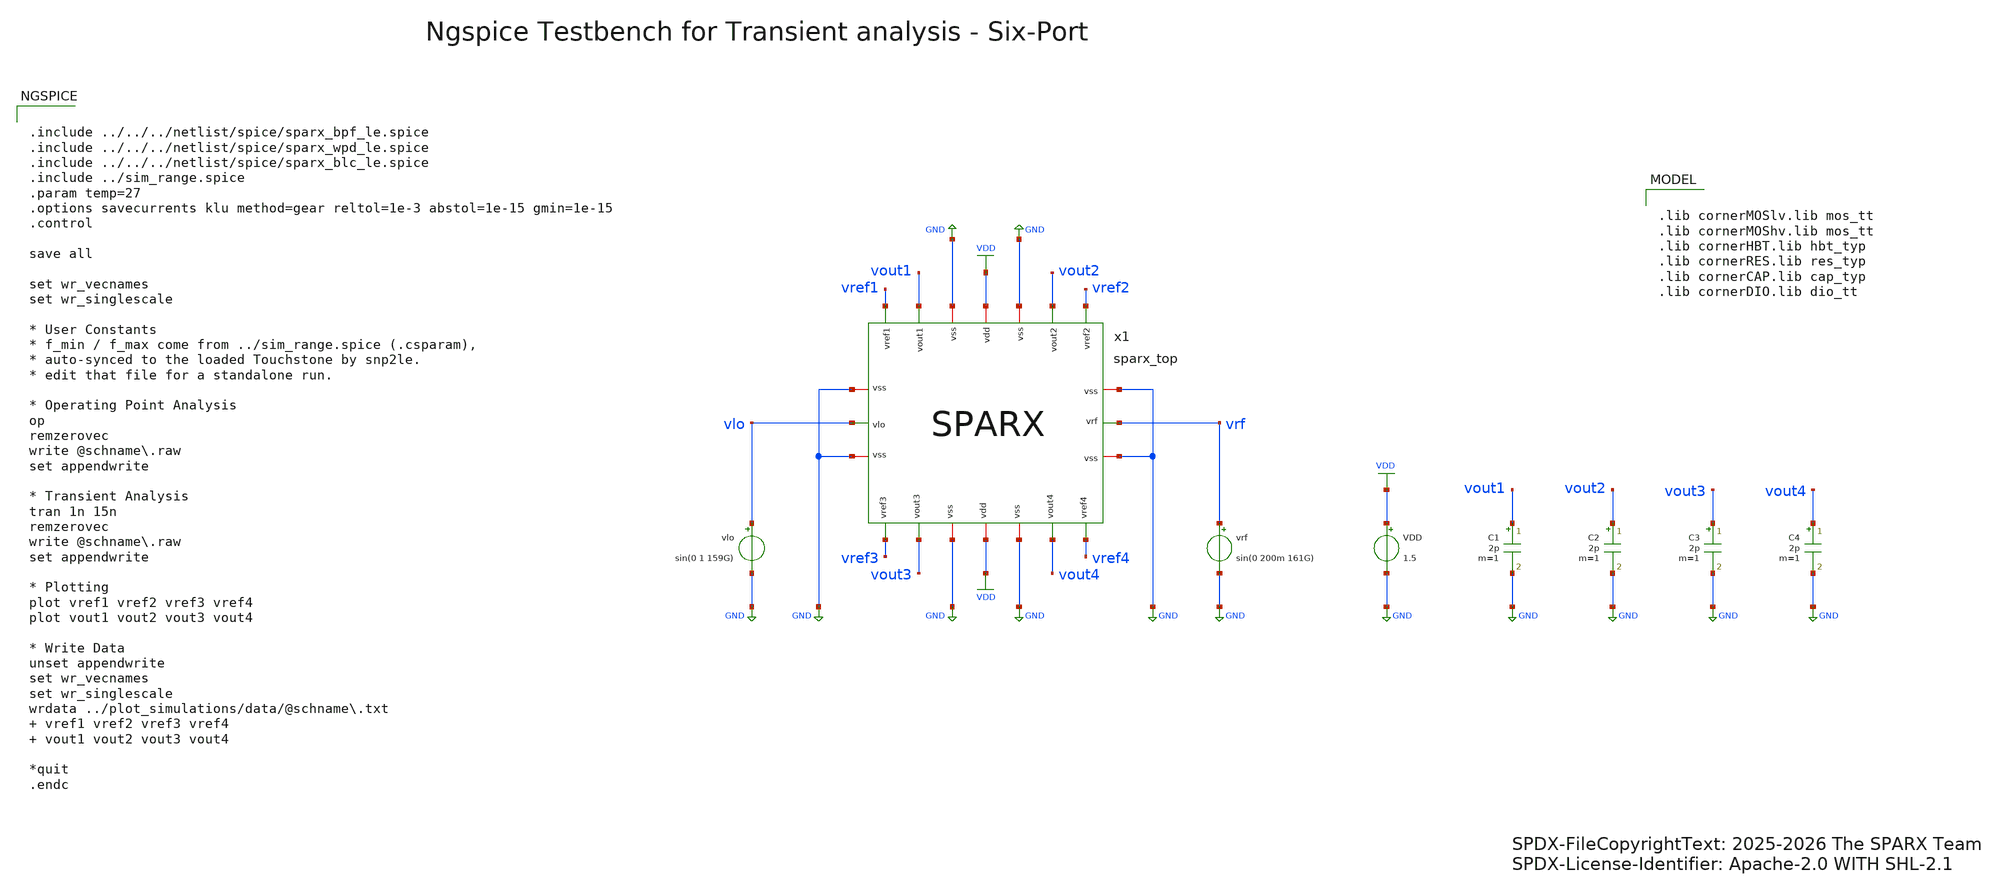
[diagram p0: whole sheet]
** sch_path: testbenches/xschem/sparx_top_tb_tran_ngspice.sch
* SPDX-FileCopyrightText: 2025-2026 The SPARX Team
* SPDX-License-Identifier: Apache-2.0 WITH SHL-2.1
**.subckt sparx_top_tb_tran_ngspice
vlo vlo GND sin(0 1 159G)
vrf vrf GND sin(0 200m 161G)
x1 vout2 vout1 VDD GND vref1 vref2 vrf vlo vout4 vref4 vref3 vout3 sparx_top
VDD VDD GND 1.5
C1 vout1 GND 2p m=1
C2 vout2 GND 2p m=1
C3 vout3 GND 2p m=1
C4 vout4 GND 2p m=1
**** begin user architecture code


.include ../../../netlist/spice/sparx_bpf_le.spice
.include ../../../netlist/spice/sparx_wpd_le.spice
.include ../../../netlist/spice/sparx_blc_le.spice
.include ../sim_range.spice
.param temp=27
.options savecurrents klu method=gear reltol=1e-3 abstol=1e-15 gmin=1e-15
.control

save all

set wr_vecnames
set wr_singlescale

* User Constants
* f_min / f_max come from ../sim_range.spice (.csparam),
* auto-synced to the loaded Touchstone by snp2le.
* edit that file for a standalone run.

* Operating Point Analysis
op
remzerovec
write @schname\.raw
set appendwrite

* Transient Analysis
tran 1n 15n
remzerovec
write @schname\.raw
set appendwrite

* Plotting
plot vref1 vref2 vref3 vref4
plot vout1 vout2 vout3 vout4

* Write Data
unset appendwrite
set wr_vecnames
set wr_singlescale
wrdata ../plot_simulations/data/@schname\.txt  vref1 vref2 vref3 vref4  vout1 vout2 vout3 vout4

*quit
.endc



.lib cornerMOSlv.lib mos_tt
.lib cornerMOShv.lib mos_tt
.lib cornerHBT.lib hbt_typ
.lib cornerRES.lib res_typ
.lib cornerCAP.lib cap_typ
.lib cornerDIO.lib dio_tt

**** end user architecture code
**.ends
.GLOBAL GND
.GLOBAL VDD
.end
